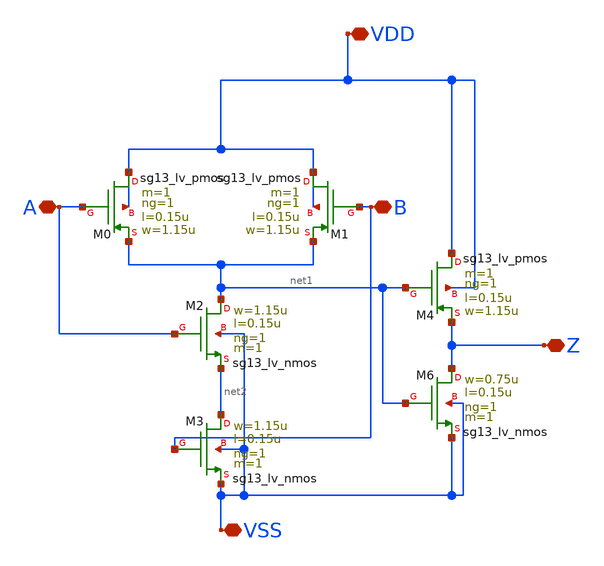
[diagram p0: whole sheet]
** sch_path: blocks/and-g/and-g.sch
**.subckt and-g VDD Z A B VSS
*.iopin VDD
*.iopin Z
*.iopin A
*.iopin B
*.iopin VSS
XM0 VDD A net1 VDD sg13_lv_pmos w=1.15u l=0.15u ng=1 m=1 mm_ok=1
XM1 VDD B net1 VDD sg13_lv_pmos w=1.15u l=0.15u ng=1 m=1 mm_ok=1
XM4 VDD net1 Z VDD sg13_lv_pmos w=1.15u l=0.15u ng=1 m=1 mm_ok=1
XM6 Z net1 VSS VSS sg13_lv_nmos w=0.75u l=0.15u ng=1 m=1 mm_ok=1
XM2 net1 A net2 VSS sg13_lv_nmos w=1.15u l=0.15u ng=1 m=1 mm_ok=1
XM3 net2 B VSS VSS sg13_lv_nmos w=1.15u l=0.15u ng=1 m=1 mm_ok=1
**.ends
.end
